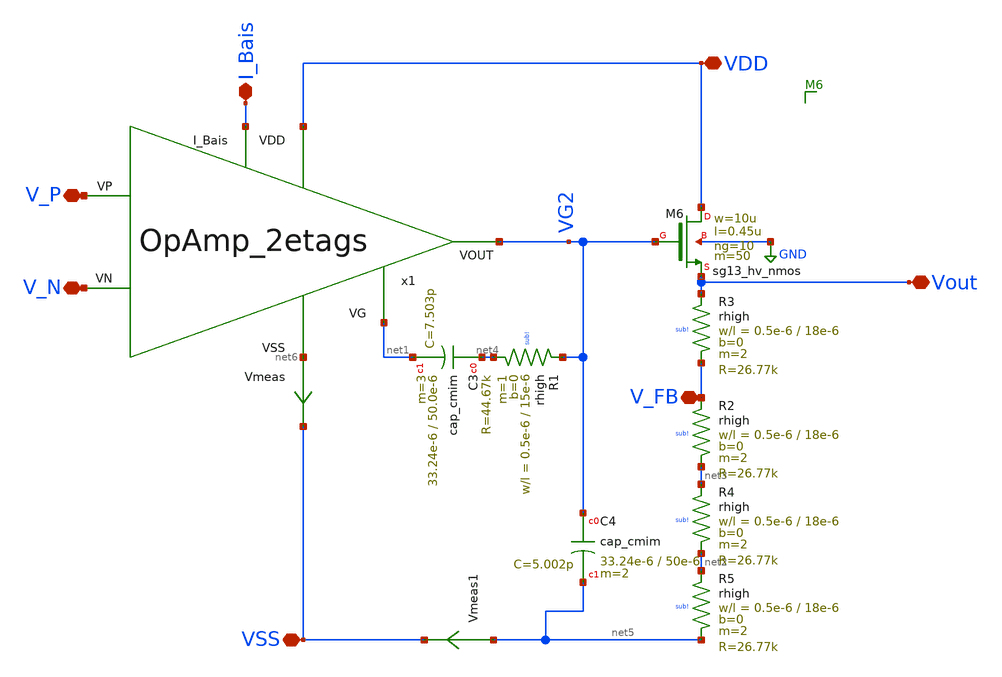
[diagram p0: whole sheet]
** sch_path: dependencies/PMU/PMU-main/schematic/xschem/LDO_NMOS_1V2.sch
**.subckt LDO_NMOS_1V2 Vout VDD I_Bais V_P V_N V_FB VSS
*.iopin Vout
*.iopin VDD
*.iopin I_Bais
*.iopin V_P
*.iopin V_N
*.iopin V_FB
*.iopin VSS
Vmeas net6 VSS 0
.save i(vmeas)
XM6 VDD VG2 Vout GND sg13_hv_nmos w=10u l=0.45u ng=10 m=50 mm_ok=1
XR3 Vout V_FB sub! rhigh w=0.5e-6 l=18e-6 m=2 b=0 mm_ok=1
Vmeas1 net5 VSS 0
.save i(vmeas1)
XR2 V_FB net3 sub! rhigh w=0.5e-6 l=18e-6 m=2 b=0 mm_ok=1
XR4 net3 net2 sub! rhigh w=0.5e-6 l=18e-6 m=2 b=0 mm_ok=1
XR5 net2 net5 sub! rhigh w=0.5e-6 l=18e-6 m=2 b=0 mm_ok=1
x1 VDD I_Bais V_N V_P net1 VG2 net6 OpAmp_2etags
XC3 net4 net1 cap_cmim w=33.24e-6 l=50.0e-6 m=3 mm_ok=1
XC4 VG2 net5 cap_cmim w=33.24e-6 l=50e-6 m=2 mm_ok=1
XR1 VG2 net4 sub! rhigh w=0.5e-6 l=15e-6 m=1 b=0 mm_ok=1
**.ends

* expanding   symbol:  OpAmp_2etags.sym # of pins=7
** sym_path: dependencies/PMU/PMU-main/schematic/xschem/OpAmp_2etags.sym
** sch_path: dependencies/PMU/PMU-main/schematic/xschem/OpAmp_2etags.sch
.subckt OpAmp_2etags VDD I_Bais VP VN VG VOUT VSS
*.iopin VDD
*.iopin I_Bais
*.iopin VP
*.iopin VN
*.iopin VG
*.iopin VOUT
*.iopin VSS
XM3 VX2 VX2 VSS VSS sg13_hv_nmos w=10u l=2u ng=1 m=2 mm_ok=1
XM1 VX2 VP net1 VDD sg13_hv_pmos w=5u l=2u ng=1 m=2 mm_ok=1
XM2 VG VN net1 VDD sg13_hv_pmos w=5u l=2u ng=1 m=2 mm_ok=1
XM4 VG VX2 VSS VSS sg13_hv_nmos w=10u l=2u ng=1 m=2 mm_ok=1
XM5 net1 I_Bais VDD VDD sg13_hv_pmos w=10u l=2u ng=1 m=4 mm_ok=1
XM7 VOUT I_Bais VDD VDD sg13_hv_pmos w=10u l=2u ng=1 m=8 mm_ok=1
XM6 VOUT VG VSS VSS sg13_hv_nmos w=10u l=2u ng=1 m=8 mm_ok=1
.ends

.GLOBAL GND
.end
